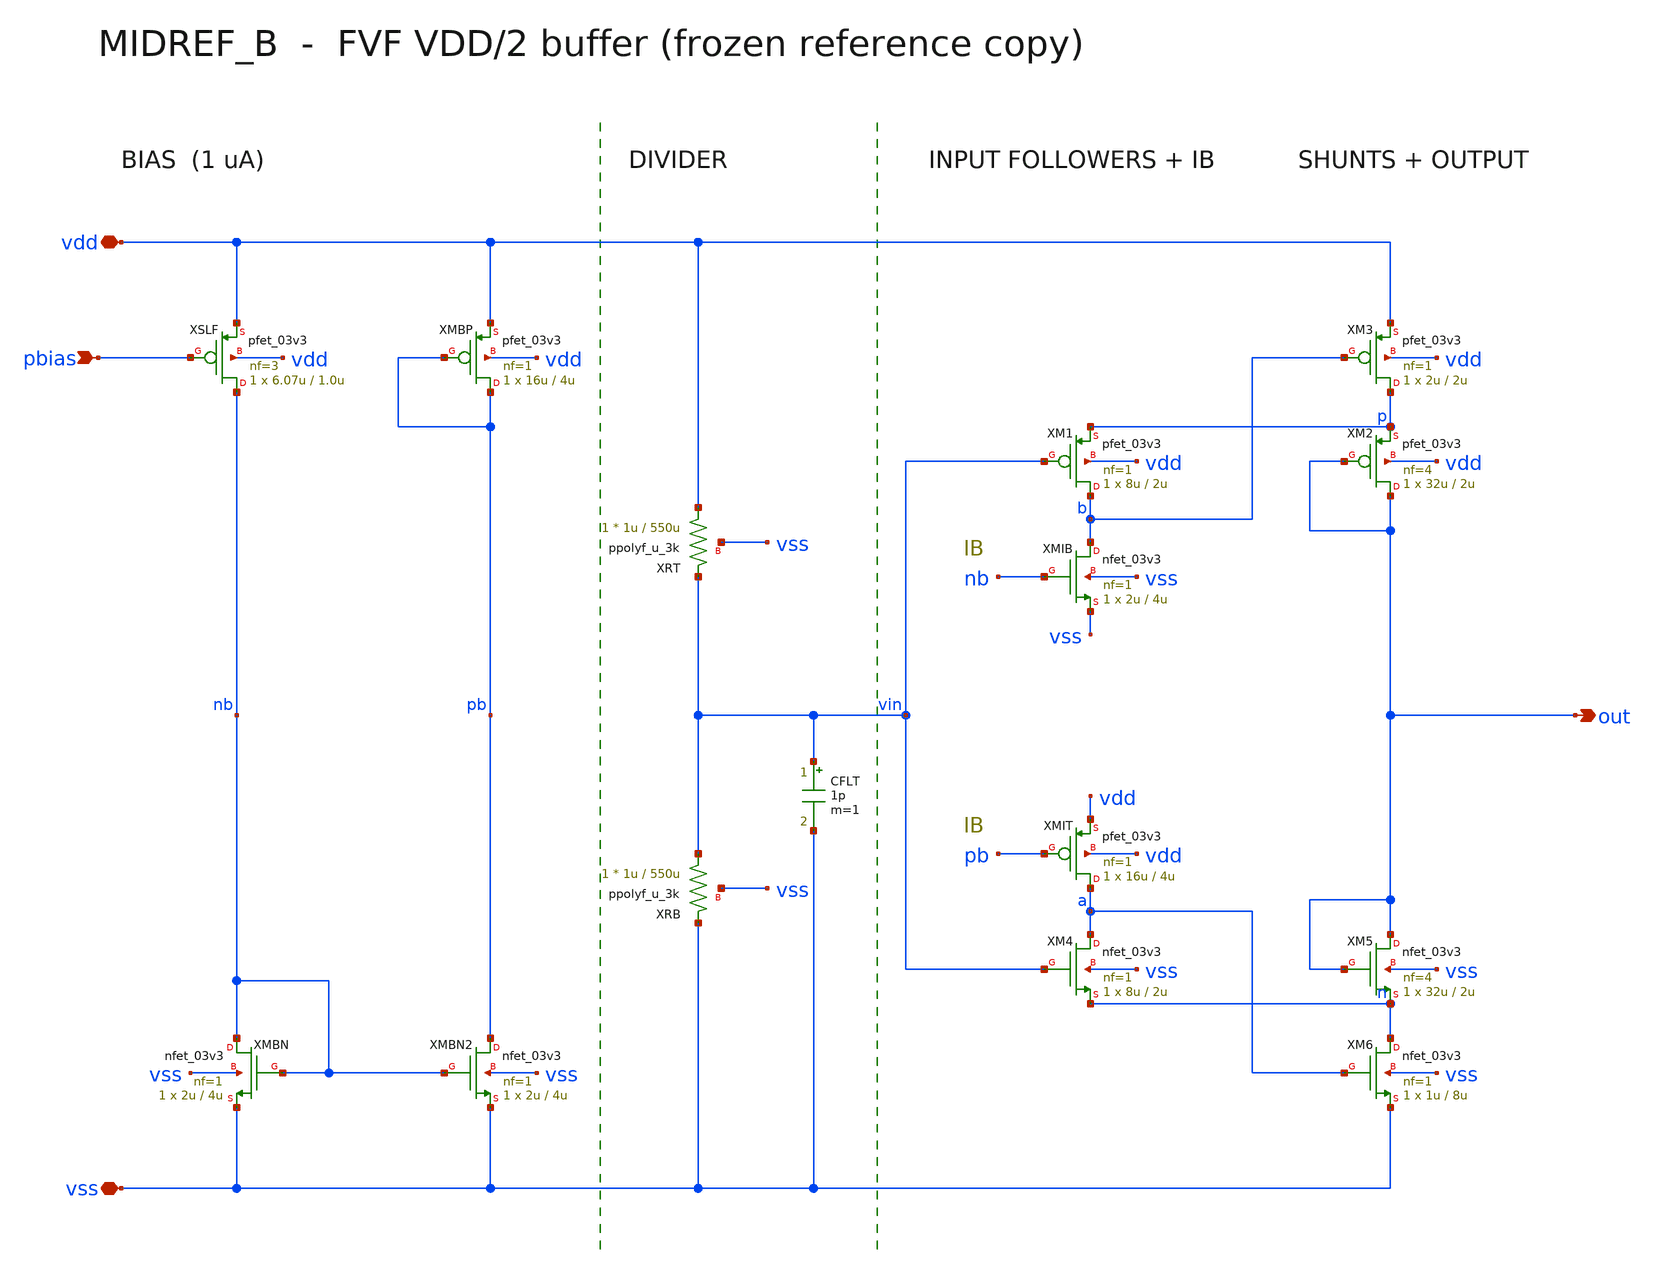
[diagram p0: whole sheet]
** sch_path: mixed_signal/ramp_gen/ref/midrail_ref/midref_b.sch
**.subckt midref_b vdd vss pbias out
*.iopin vdd
*.iopin vss
*.ipin pbias
*.opin out
XSLF nb pbias vdd vdd pfet_03v3 L=1.0u W=6.07u nf=3 m=1
XMBP pb pb vdd vdd pfet_03v3 L=4u W=16u nf=1 m=1
XMBN nb nb vss vss nfet_03v3 L=4u W=2u nf=1 m=1
XMBN2 pb nb vss vss nfet_03v3 L=4u W=2u nf=1 m=1
XRT vdd vin vss ppolyf_u_3k r_width=1u r_length=550u m=1
XRB vin vss vss ppolyf_u_3k r_width=1u r_length=550u m=1
CFLT vin vss 1p m=1
XM1 b vin p vdd pfet_03v3 L=2u W=8u nf=1 m=1
XMIB b nb vss vss nfet_03v3 L=4u W=2u nf=1 m=1
XMIT a pb vdd vdd pfet_03v3 L=4u W=16u nf=1 m=1
XM4 a vin n vss nfet_03v3 L=2u W=8u nf=1 m=1
XM3 p b vdd vdd pfet_03v3 L=2u W=2u nf=1 m=1
XM2 out out p vdd pfet_03v3 L=2u W=32u nf=4 m=1
XM5 out out n vss nfet_03v3 L=2u W=32u nf=4 m=1
XM6 n a vss vss nfet_03v3 L=8u W=1u nf=1 m=1
**.ends
.end
